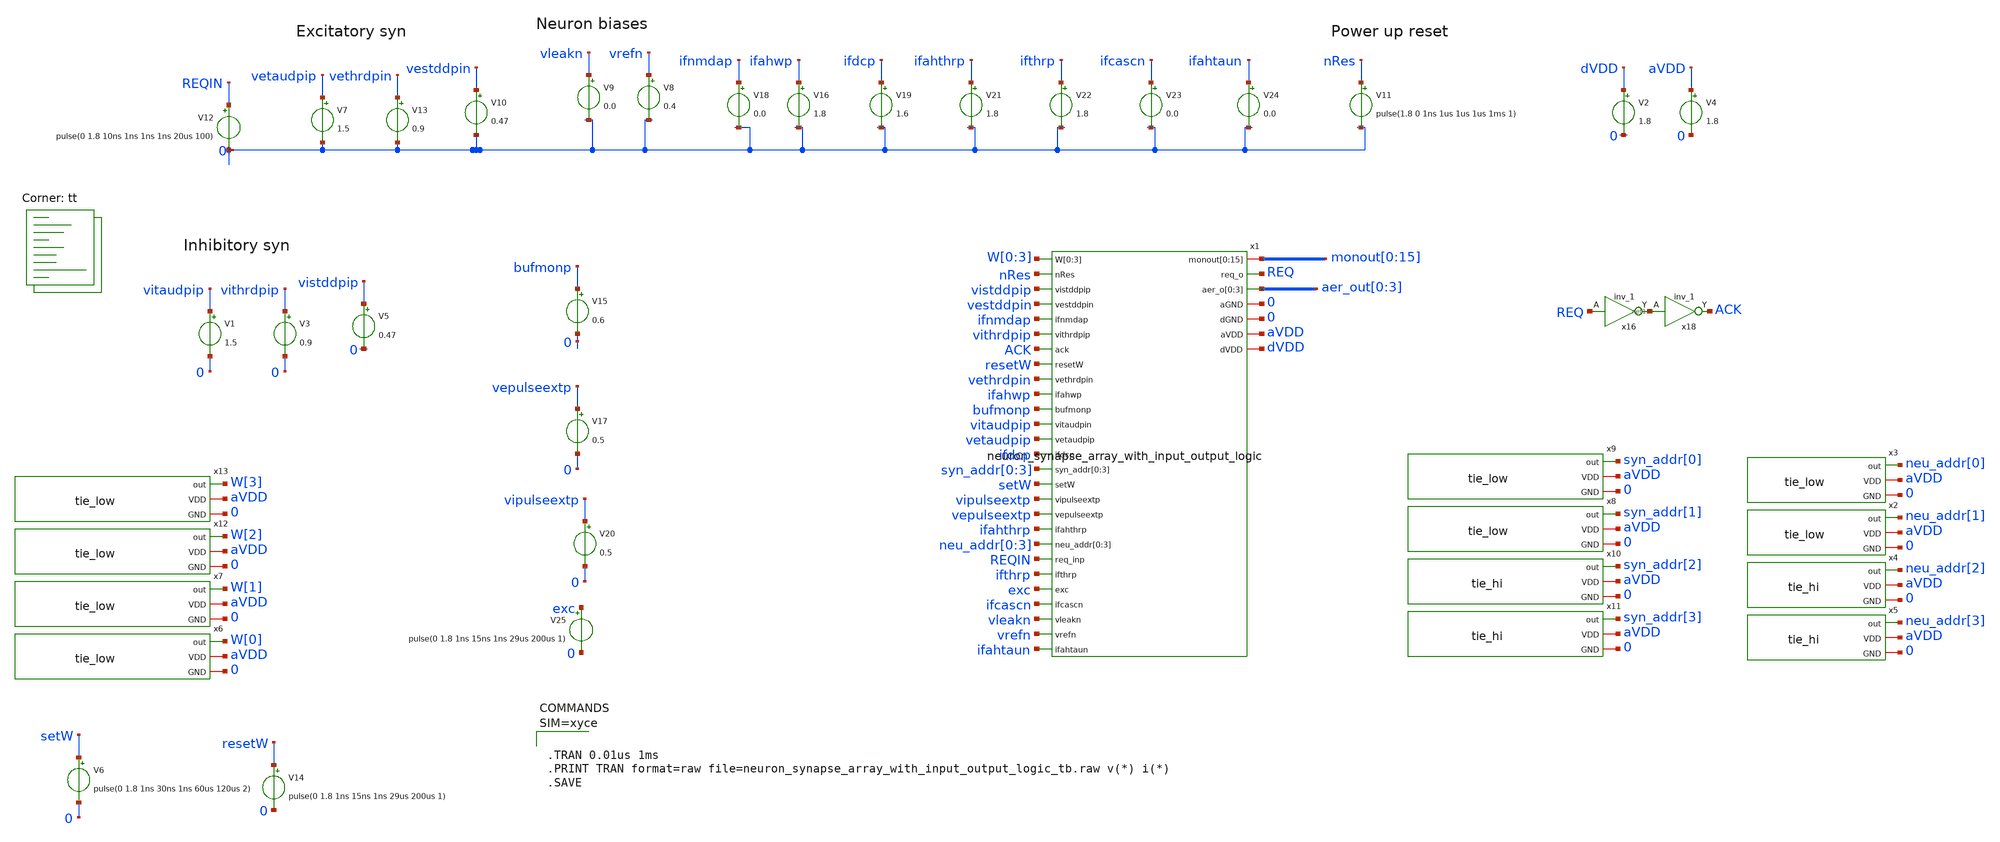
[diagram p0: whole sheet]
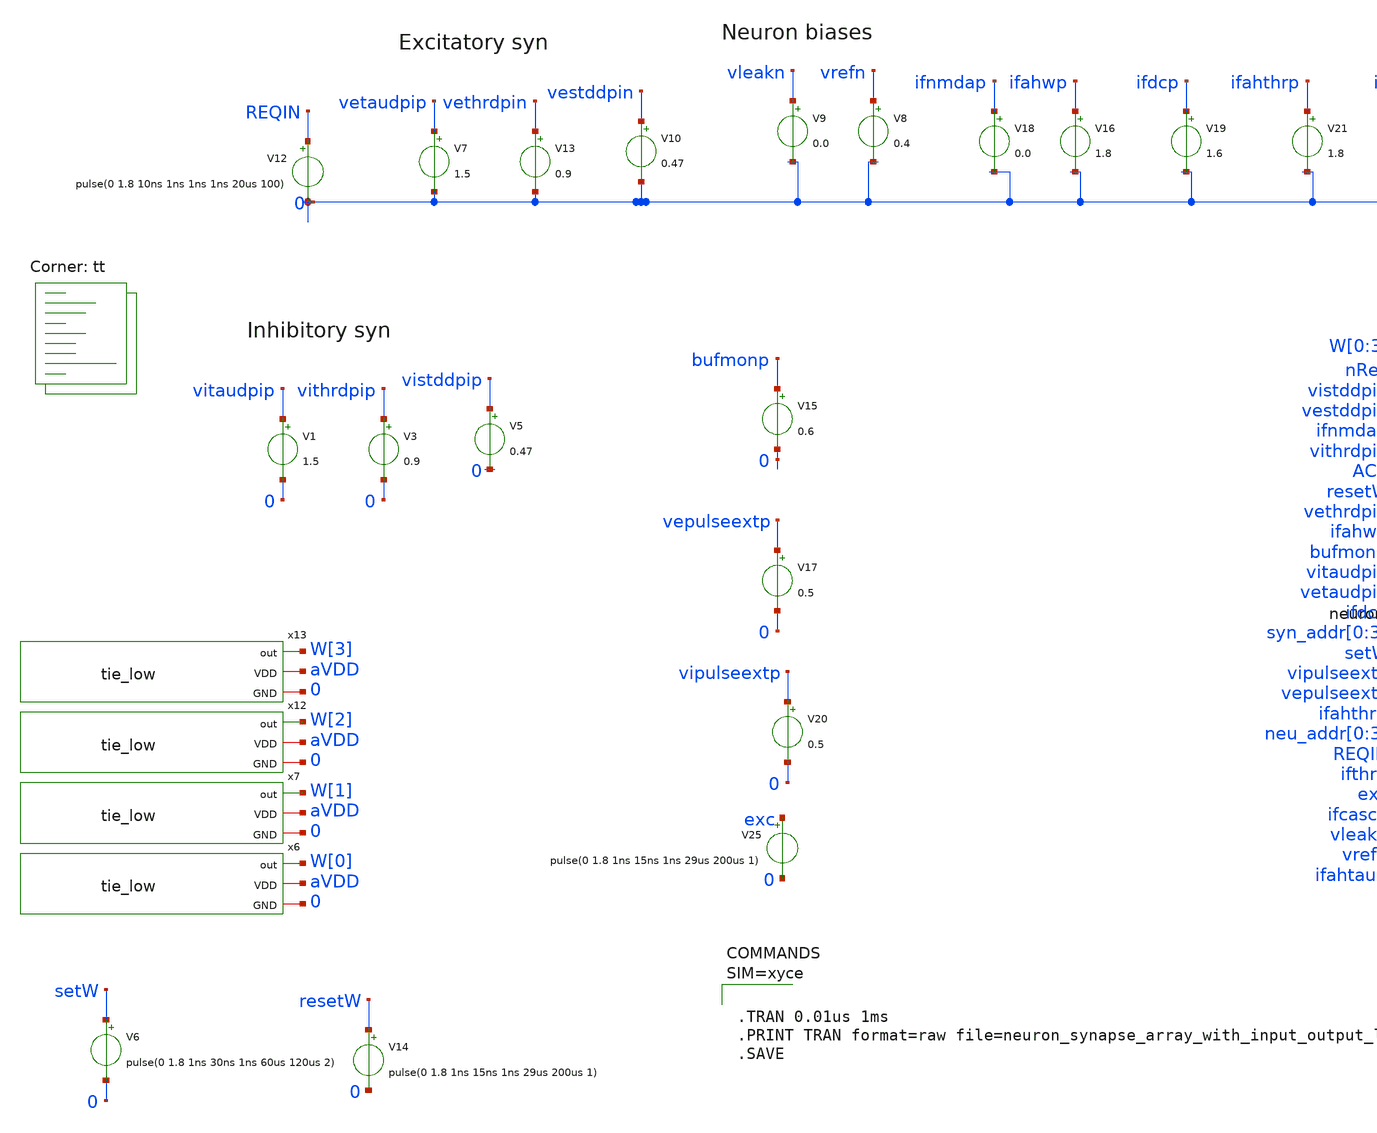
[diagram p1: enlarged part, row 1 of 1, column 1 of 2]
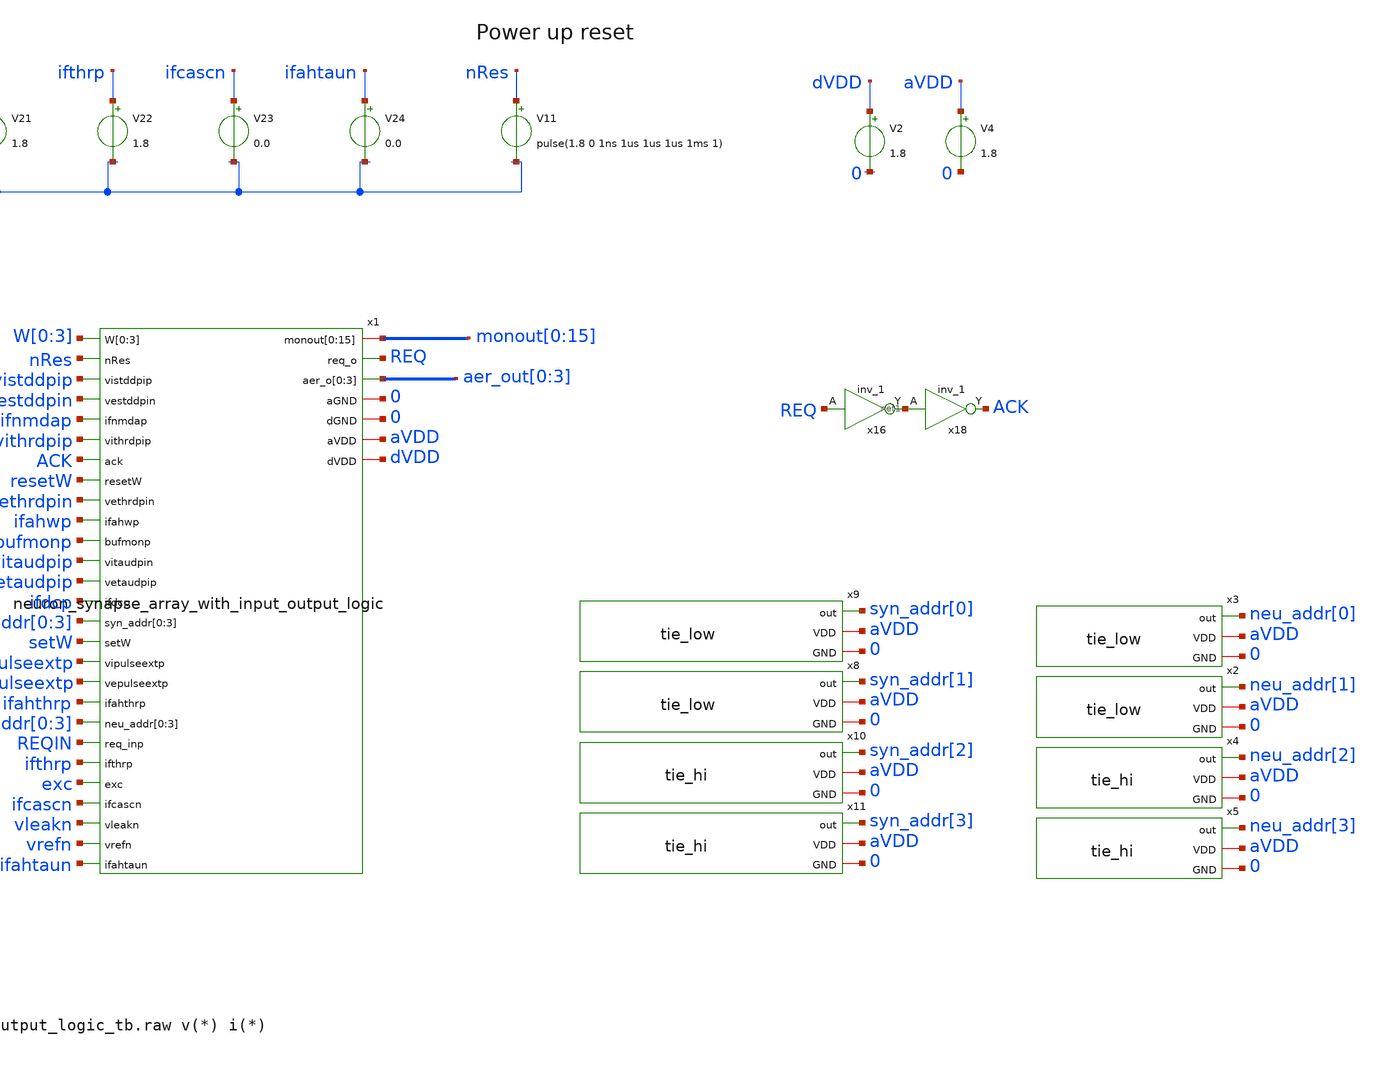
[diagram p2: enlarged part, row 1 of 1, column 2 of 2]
** sch_path: design/xschem/neuron_synapse_array_with_input_output_logic_tb.sch
**.subckt neuron_synapse_array_with_input_output_logic_tb
x1 W[0] W[1] W[2] W[3] nRes vistddpip vestddpin ifnmdap monout[0] monout[1] monout[2] monout[3]
+ monout[4] monout[5] monout[6] monout[7] monout[8] monout[9] monout[10] monout[11] monout[12] monout[13]
+ monout[14] monout[15] REQ vithrdpip ACK resetW vethrdpin ifahwp aer_out[0] aer_out[1] aer_out[2] aer_out[3]
+ bufmonp vitaudpip vetaudpip ifdcp syn_addr[0] syn_addr[1] syn_addr[2] syn_addr[3] setW vipulseextp
+ vepulseextp ifahthrp neu_addr[0] neu_addr[1] neu_addr[2] neu_addr[3] REQIN ifthrp exc ifcascn 0 0 vleakn aVDD
+ dVDD vrefn ifahtaun neuron_synapse_array_with_input_output_logic
V2 dVDD 0 1.8
V8 vrefn 0 0.4
V9 vleakn 0 0.0
V16 ifahwp 0 1.8
V18 ifnmdap 0 0.0
V19 ifdcp 0 1.6
V21 ifahthrp 0 1.8
V22 ifthrp 0 1.8
V23 ifcascn 0 0.0
V24 ifahtaun 0 0.0
V7 vetaudpip 0 1.5
V13 vethrdpin 0 0.9
V10 vestddpin 0 0.47
V12 REQIN 0 pulse(0 1.8 10ns 1ns 1ns 1ns 20us 100)
V4 aVDD 0 1.8
V11 nRes 0 pulse(1.8 0 1ns 1us 1us 1us 1ms 1)
V1 vitaudpip 0 1.5
V3 vithrdpip 0 0.9
V5 vistddpip 0 0.47
V15 bufmonp 0 0.6
x6 W[0] aVDD 0 tie_low
x7 W[1] aVDD 0 tie_low
V6 setW 0 pulse(0 1.8 1ns 30ns 1ns 60us 120us 2)
V14 resetW 0 pulse(0 1.8 1ns 15ns 1ns 29us 200us 1)
V17 vepulseextp 0 0.5
V20 vipulseextp 0 0.5
V25 exc 0 pulse(0 1.8 1ns 15ns 1ns 29us 200us 1)
x16 REQ 0 0 dVDD dVDD net1 sky130_fd_sc_hd__inv_1
x18 net1 0 0 dVDD dVDD ACK sky130_fd_sc_hd__inv_1
x8 syn_addr[1] aVDD 0 tie_low
x9 syn_addr[0] aVDD 0 tie_low
x10 syn_addr[2] aVDD 0 tie_hi
x11 syn_addr[3] aVDD 0 tie_hi
x2 neu_addr[1] aVDD 0 tie_low
x3 neu_addr[0] aVDD 0 tie_low
x4 neu_addr[2] aVDD 0 tie_hi
x5 neu_addr[3] aVDD 0 tie_hi
x12 W[2] aVDD 0 tie_low
x13 W[3] aVDD 0 tie_low
**** begin user architecture code


* Standard cell simulation files
.include $::SKYWATER_STDCELLS/sky130_fd_sc_hd.spice


.lib $::SKYWATER_MODELS/sky130.lib.spice tt



**** end user architecture code
**.ends
.end
